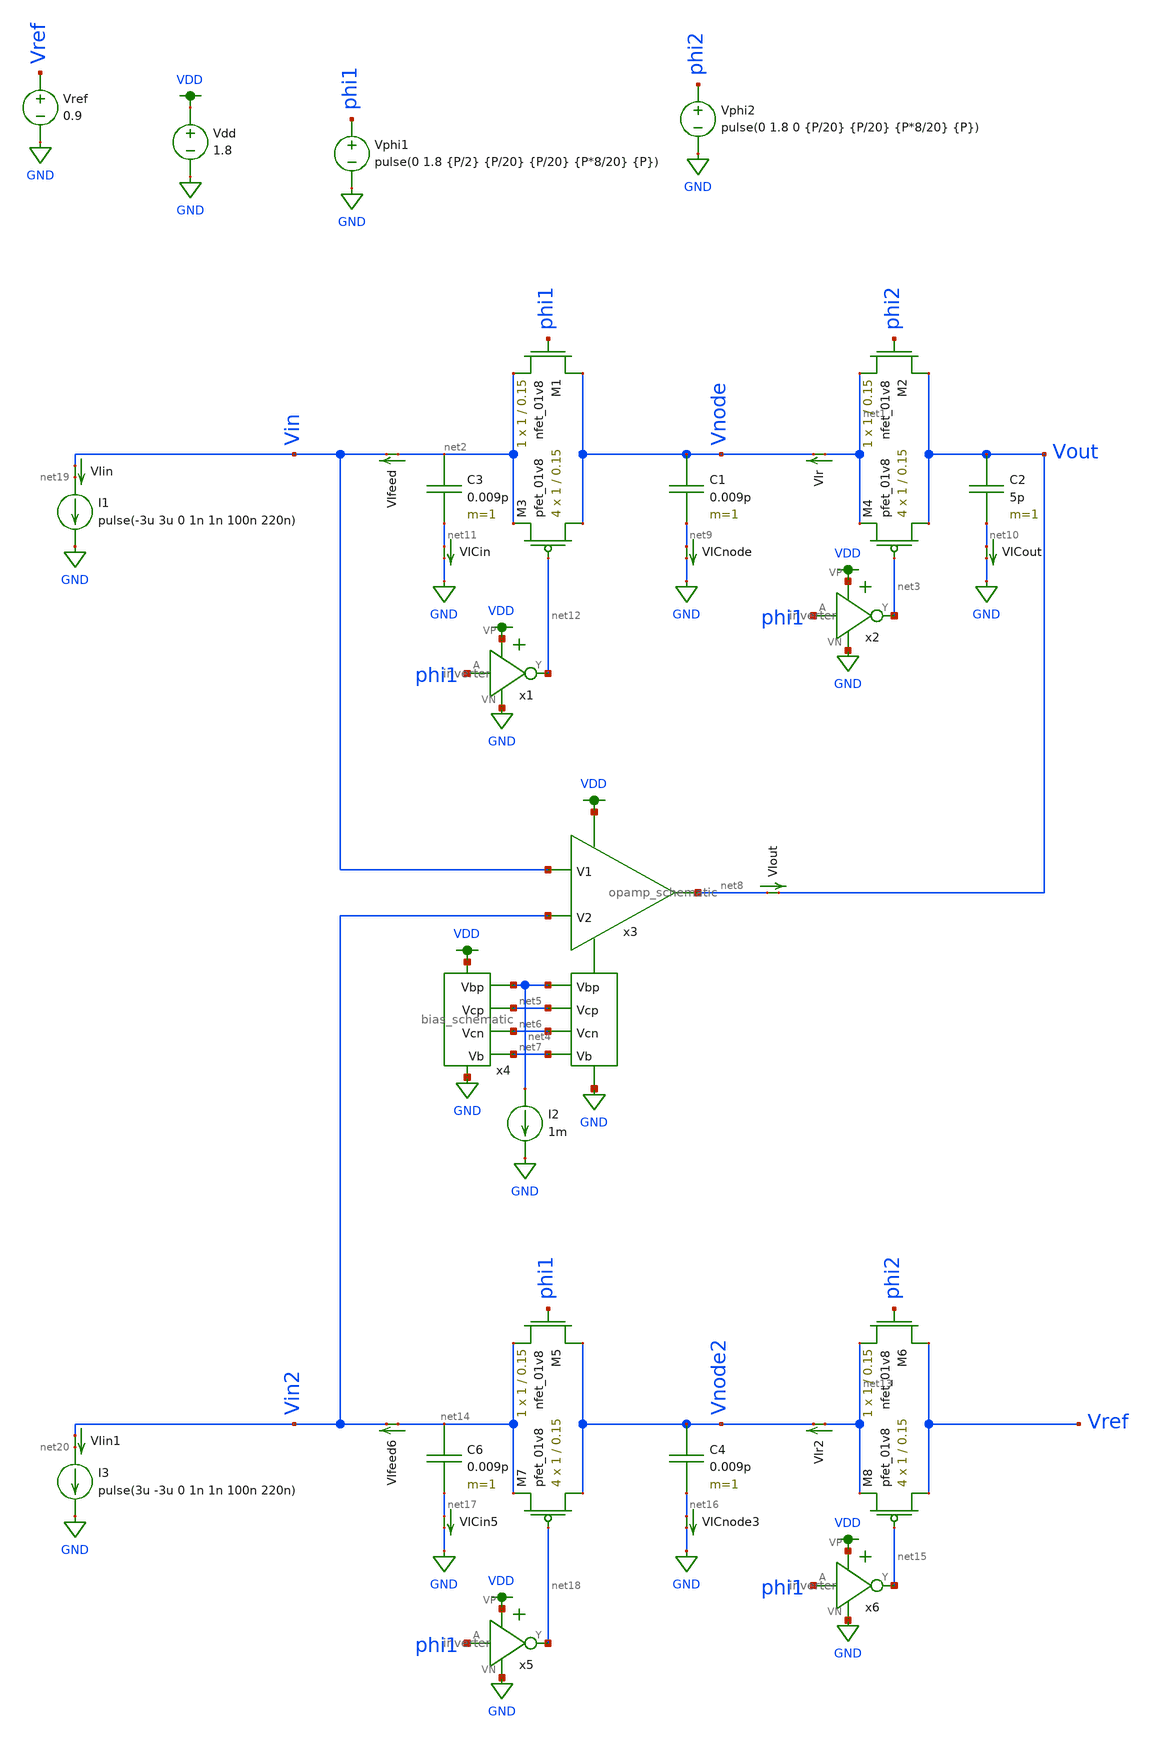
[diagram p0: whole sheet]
** sch_path: xschem/switched_capacitor/switched_capacitor_dual_iv_converter.sch
**.subckt switched_capacitor_dual_iv_converter
C1 Vnode net9 0.009p m=1
XM1 Vnode phi1 net2 GND sky130_fd_pr__nfet_01v8 L=0.15 W=1 nf=1 ad='int((nf+1)/2) * W/nf * 0.29' as='int((nf+2)/2) * W/nf * 0.29'
+ pd='2*int((nf+1)/2) * (W/nf + 0.29)' ps='2*int((nf+2)/2) * (W/nf + 0.29)' nrd='0.29 / W' nrs='0.29 / W'
+ sa=0 sb=0 sd=0 mult=1 m=1
XM2 Vout phi2 net1 GND sky130_fd_pr__nfet_01v8 L=0.15 W=1 nf=1 ad='int((nf+1)/2) * W/nf * 0.29' as='int((nf+2)/2) * W/nf * 0.29'
+ pd='2*int((nf+1)/2) * (W/nf + 0.29)' ps='2*int((nf+2)/2) * (W/nf + 0.29)' nrd='0.29 / W' nrs='0.29 / W'
+ sa=0 sb=0 sd=0 mult=1 m=1
Vphi1 phi1 GND pulse(0 1.8 {P/2} {P/20} {P/20} {P*8/20} {P})
Vphi2 phi2 GND pulse(0 1.8 0 {P/20} {P/20} {P*8/20} {P})
Vdd VDD GND 1.8
C2 Vout net10 5p m=1
XM3 Vnode net12 net2 VDD sky130_fd_pr__pfet_01v8 L=0.15 W=1 nf=1 ad='int((nf+1)/2) * W/nf * 0.29' as='int((nf+2)/2) * W/nf * 0.29'
+ pd='2*int((nf+1)/2) * (W/nf + 0.29)' ps='2*int((nf+2)/2) * (W/nf + 0.29)' nrd='0.29 / W' nrs='0.29 / W'
+ sa=0 sb=0 sd=0 mult=4 m=4
XM4 Vout net3 net1 VDD sky130_fd_pr__pfet_01v8 L=0.15 W=1 nf=1 ad='int((nf+1)/2) * W/nf * 0.29' as='int((nf+2)/2) * W/nf * 0.29'
+ pd='2*int((nf+1)/2) * (W/nf + 0.29)' ps='2*int((nf+2)/2) * (W/nf + 0.29)' nrd='0.29 / W' nrs='0.29 / W'
+ sa=0 sb=0 sd=0 mult=4 m=4
x1 VDD phi1 net12 GND inverter
x2 VDD phi1 net3 GND inverter
I1 net19 GND pulse(-3u 3u 0 1n 1n 100n 220n)
C3 net2 net11 0.009p m=1
x3 VDD net4 net5 net8 Vin Vin2 net6 net7 GND opamp_schematic
x4 VDD net4 net5 net6 GND net7 bias_schematic
Vref Vref GND 0.9
I2 net4 GND 1m
VIin Vin net19 0
.save i(viin)
VIr net1 Vnode 0
.save i(vir)
VIout net8 Vout 0
.save i(viout)
VICnode net9 GND 0
.save i(vicnode)
VICout net10 GND 0
.save i(vicout)
VICin net11 GND 0
.save i(vicin)
VIfeed net2 Vin 0
.save i(vifeed)
C4 Vnode2 net16 0.009p m=1
XM5 Vnode2 phi1 net14 GND sky130_fd_pr__nfet_01v8 L=0.15 W=1 nf=1 ad='int((nf+1)/2) * W/nf * 0.29' as='int((nf+2)/2) * W/nf * 0.29'
+ pd='2*int((nf+1)/2) * (W/nf + 0.29)' ps='2*int((nf+2)/2) * (W/nf + 0.29)' nrd='0.29 / W' nrs='0.29 / W'
+ sa=0 sb=0 sd=0 mult=1 m=1
XM6 Vref phi2 net13 GND sky130_fd_pr__nfet_01v8 L=0.15 W=1 nf=1 ad='int((nf+1)/2) * W/nf * 0.29' as='int((nf+2)/2) * W/nf * 0.29'
+ pd='2*int((nf+1)/2) * (W/nf + 0.29)' ps='2*int((nf+2)/2) * (W/nf + 0.29)' nrd='0.29 / W' nrs='0.29 / W'
+ sa=0 sb=0 sd=0 mult=1 m=1
XM7 Vnode2 net18 net14 VDD sky130_fd_pr__pfet_01v8 L=0.15 W=1 nf=1 ad='int((nf+1)/2) * W/nf * 0.29' as='int((nf+2)/2) * W/nf * 0.29'
+ pd='2*int((nf+1)/2) * (W/nf + 0.29)' ps='2*int((nf+2)/2) * (W/nf + 0.29)' nrd='0.29 / W' nrs='0.29 / W'
+ sa=0 sb=0 sd=0 mult=4 m=4
XM8 Vref net15 net13 VDD sky130_fd_pr__pfet_01v8 L=0.15 W=1 nf=1 ad='int((nf+1)/2) * W/nf * 0.29' as='int((nf+2)/2) * W/nf * 0.29'
+ pd='2*int((nf+1)/2) * (W/nf + 0.29)' ps='2*int((nf+2)/2) * (W/nf + 0.29)' nrd='0.29 / W' nrs='0.29 / W'
+ sa=0 sb=0 sd=0 mult=4 m=4
x5 VDD phi1 net18 GND inverter
x6 VDD phi1 net15 GND inverter
I3 net20 GND pulse(3u -3u 0 1n 1n 100n 220n)
C6 net14 net17 0.009p m=1
VIin1 Vin2 net20 0
.save i(viin1)
VIr2 net13 Vnode2 0
.save i(vir2)
VICnode3 net16 GND 0
.save i(vicnode3)
VICin5 net17 GND 0
.save i(vicin5)
VIfeed6 net14 Vin2 0
.save i(vifeed6)
**** begin user architecture code

.option wnflag=1
.param MC_SWITCH=0.0
.lib ~/skywater/skywater-pdk/libraries/sky130_fd_pr_ngspice/latest/models/sky130.lib.spice tt


.param P=10n
.save all
.control
save all
nodeset v(Vout)=0.9
tran 0.005n 500n
run
plot v(Vin) v(Vout) v(Vnode) v(phi2)
plot i(VIin) i(VIr)
plot v(Vout) i(VIin)*50000+v(Vref)
plot i(VIin) i(VIfeed) i(VIout)
plot i(VICin) i(VICnode) i(VICout)
.endc

**** end user architecture code
**.ends

* expanding   symbol:  /home/madvlsi/dev/git/magic-dds/xschem/other_project_files/inverter.sym # of
*+ pins=4
** sym_path: xschem/other_project_files/inverter.sym
** sch_path: xschem/other_project_files/inverter.sch
.subckt inverter VP A Y VN
*.iopin VP
*.iopin VN
*.ipin A
*.opin Y
XM1 Y A VN VN sky130_fd_pr__nfet_01v8 L=0.15 W=1 nf=1 ad='int((nf+1)/2) * W/nf * 0.29' as='int((nf+2)/2) * W/nf * 0.29'
+ pd='2*int((nf+1)/2) * (W/nf + 0.29)' ps='2*int((nf+2)/2) * (W/nf + 0.29)' nrd='0.29 / W' nrs='0.29 / W'
+ sa=0 sb=0 sd=0 mult=1 m=1
XM2 Y A VP VP sky130_fd_pr__pfet_01v8 L=0.15 W=4 nf=1 ad='int((nf+1)/2) * W/nf * 0.29' as='int((nf+2)/2) * W/nf * 0.29'
+ pd='2*int((nf+1)/2) * (W/nf + 0.29)' ps='2*int((nf+2)/2) * (W/nf + 0.29)' nrd='0.29 / W' nrs='0.29 / W'
+ sa=0 sb=0 sd=0 mult=1 m=1
.ends


* expanding   symbol:
*+  /home/madvlsi/dev/git/magic-dds/xschem/other_project_files/opamp_schematic.sym # of pins=9
** sym_path: xschem/other_project_files/opamp_schematic.sym
** sch_path: xschem/other_project_files/opamp_schematic.sch
.subckt opamp_schematic VP Vbp Vcp Vout V1 V2 Vcn Vb VN
*.ipin Vbp
*.ipin Vcp
*.ipin Vcn
*.ipin V2
*.ipin V1
*.ipin Vb
*.iopin VP
*.iopin VN
*.opin Vout
XM1a M1top V1 Vnode GND sky130_fd_pr__nfet_01v8 L=0.5 W=3 nf=1 ad='int((nf+1)/2) * W/nf * 0.29' as='int((nf+2)/2) * W/nf * 0.29'
+ pd='2*int((nf+1)/2) * (W/nf + 0.29)' ps='2*int((nf+2)/2) * (W/nf + 0.29)' nrd='0.29 / W' nrs='0.29 / W'
+ sa=0 sb=0 sd=0 mult=1 m=1
XM1b M1top V1 Vnode GND sky130_fd_pr__nfet_01v8 L=0.5 W=3 nf=1 ad='int((nf+1)/2) * W/nf * 0.29' as='int((nf+2)/2) * W/nf * 0.29'
+ pd='2*int((nf+1)/2) * (W/nf + 0.29)' ps='2*int((nf+2)/2) * (W/nf + 0.29)' nrd='0.29 / W' nrs='0.29 / W'
+ sa=0 sb=0 sd=0 mult=1 m=1
XM1c M1top V1 Vnode GND sky130_fd_pr__nfet_01v8 L=0.5 W=3 nf=1 ad='int((nf+1)/2) * W/nf * 0.29' as='int((nf+2)/2) * W/nf * 0.29'
+ pd='2*int((nf+1)/2) * (W/nf + 0.29)' ps='2*int((nf+2)/2) * (W/nf + 0.29)' nrd='0.29 / W' nrs='0.29 / W'
+ sa=0 sb=0 sd=0 mult=1 m=1
XM1d M1top V1 Vnode GND sky130_fd_pr__nfet_01v8 L=0.5 W=3 nf=1 ad='int((nf+1)/2) * W/nf * 0.29' as='int((nf+2)/2) * W/nf * 0.29'
+ pd='2*int((nf+1)/2) * (W/nf + 0.29)' ps='2*int((nf+2)/2) * (W/nf + 0.29)' nrd='0.29 / W' nrs='0.29 / W'
+ sa=0 sb=0 sd=0 mult=1 m=1
XM2a M2top V2 Vnode GND sky130_fd_pr__nfet_01v8 L=0.5 W=3 nf=1 ad='int((nf+1)/2) * W/nf * 0.29' as='int((nf+2)/2) * W/nf * 0.29'
+ pd='2*int((nf+1)/2) * (W/nf + 0.29)' ps='2*int((nf+2)/2) * (W/nf + 0.29)' nrd='0.29 / W' nrs='0.29 / W'
+ sa=0 sb=0 sd=0 mult=1 m=1
XM2b M2top V2 Vnode GND sky130_fd_pr__nfet_01v8 L=0.5 W=3 nf=1 ad='int((nf+1)/2) * W/nf * 0.29' as='int((nf+2)/2) * W/nf * 0.29'
+ pd='2*int((nf+1)/2) * (W/nf + 0.29)' ps='2*int((nf+2)/2) * (W/nf + 0.29)' nrd='0.29 / W' nrs='0.29 / W'
+ sa=0 sb=0 sd=0 mult=1 m=1
XM2c M2top V2 Vnode GND sky130_fd_pr__nfet_01v8 L=0.5 W=3 nf=1 ad='int((nf+1)/2) * W/nf * 0.29' as='int((nf+2)/2) * W/nf * 0.29'
+ pd='2*int((nf+1)/2) * (W/nf + 0.29)' ps='2*int((nf+2)/2) * (W/nf + 0.29)' nrd='0.29 / W' nrs='0.29 / W'
+ sa=0 sb=0 sd=0 mult=1 m=1
XM2d M2top V2 Vnode GND sky130_fd_pr__nfet_01v8 L=0.5 W=3 nf=1 ad='int((nf+1)/2) * W/nf * 0.29' as='int((nf+2)/2) * W/nf * 0.29'
+ pd='2*int((nf+1)/2) * (W/nf + 0.29)' ps='2*int((nf+2)/2) * (W/nf + 0.29)' nrd='0.29 / W' nrs='0.29 / W'
+ sa=0 sb=0 sd=0 mult=1 m=1
XMba Vnode Vb VN GND sky130_fd_pr__nfet_01v8 L=0.5 W=1.5 nf=1 ad='int((nf+1)/2) * W/nf * 0.29' as='int((nf+2)/2) * W/nf * 0.29'
+ pd='2*int((nf+1)/2) * (W/nf + 0.29)' ps='2*int((nf+2)/2) * (W/nf + 0.29)' nrd='0.29 / W' nrs='0.29 / W'
+ sa=0 sb=0 sd=0 mult=1 m=1
XMbb Vnode Vb VN GND sky130_fd_pr__nfet_01v8 L=0.5 W=1.5 nf=1 ad='int((nf+1)/2) * W/nf * 0.29' as='int((nf+2)/2) * W/nf * 0.29'
+ pd='2*int((nf+1)/2) * (W/nf + 0.29)' ps='2*int((nf+2)/2) * (W/nf + 0.29)' nrd='0.29 / W' nrs='0.29 / W'
+ sa=0 sb=0 sd=0 mult=1 m=1
XMbc Vnode Vb VN GND sky130_fd_pr__nfet_01v8 L=0.5 W=1.5 nf=1 ad='int((nf+1)/2) * W/nf * 0.29' as='int((nf+2)/2) * W/nf * 0.29'
+ pd='2*int((nf+1)/2) * (W/nf + 0.29)' ps='2*int((nf+2)/2) * (W/nf + 0.29)' nrd='0.29 / W' nrs='0.29 / W'
+ sa=0 sb=0 sd=0 mult=1 m=1
XMbd Vnode Vb VN GND sky130_fd_pr__nfet_01v8 L=0.5 W=1.5 nf=1 ad='int((nf+1)/2) * W/nf * 0.29' as='int((nf+2)/2) * W/nf * 0.29'
+ pd='2*int((nf+1)/2) * (W/nf + 0.29)' ps='2*int((nf+2)/2) * (W/nf + 0.29)' nrd='0.29 / W' nrs='0.29 / W'
+ sa=0 sb=0 sd=0 mult=1 m=1
XMbe Vnode Vb VN GND sky130_fd_pr__nfet_01v8 L=0.5 W=1.5 nf=1 ad='int((nf+1)/2) * W/nf * 0.29' as='int((nf+2)/2) * W/nf * 0.29'
+ pd='2*int((nf+1)/2) * (W/nf + 0.29)' ps='2*int((nf+2)/2) * (W/nf + 0.29)' nrd='0.29 / W' nrs='0.29 / W'
+ sa=0 sb=0 sd=0 mult=1 m=1
XMbf Vnode Vb VN GND sky130_fd_pr__nfet_01v8 L=0.5 W=1.5 nf=1 ad='int((nf+1)/2) * W/nf * 0.29' as='int((nf+2)/2) * W/nf * 0.29'
+ pd='2*int((nf+1)/2) * (W/nf + 0.29)' ps='2*int((nf+2)/2) * (W/nf + 0.29)' nrd='0.29 / W' nrs='0.29 / W'
+ sa=0 sb=0 sd=0 mult=1 m=1
XMbg Vnode Vb VN GND sky130_fd_pr__nfet_01v8 L=0.5 W=1.5 nf=1 ad='int((nf+1)/2) * W/nf * 0.29' as='int((nf+2)/2) * W/nf * 0.29'
+ pd='2*int((nf+1)/2) * (W/nf + 0.29)' ps='2*int((nf+2)/2) * (W/nf + 0.29)' nrd='0.29 / W' nrs='0.29 / W'
+ sa=0 sb=0 sd=0 mult=1 m=1
XMbh Vnode Vb VN GND sky130_fd_pr__nfet_01v8 L=0.5 W=1.5 nf=1 ad='int((nf+1)/2) * W/nf * 0.29' as='int((nf+2)/2) * W/nf * 0.29'
+ pd='2*int((nf+1)/2) * (W/nf + 0.29)' ps='2*int((nf+2)/2) * (W/nf + 0.29)' nrd='0.29 / W' nrs='0.29 / W'
+ sa=0 sb=0 sd=0 mult=1 m=1
XM7a net2 Vcn net1 GND sky130_fd_pr__nfet_01v8 L=0.5 W=3 nf=1 ad='int((nf+1)/2) * W/nf * 0.29' as='int((nf+2)/2) * W/nf * 0.29'
+ pd='2*int((nf+1)/2) * (W/nf + 0.29)' ps='2*int((nf+2)/2) * (W/nf + 0.29)' nrd='0.29 / W' nrs='0.29 / W'
+ sa=0 sb=0 sd=0 mult=1 m=1
XM7b net2 Vcn net1 GND sky130_fd_pr__nfet_01v8 L=0.5 W=3 nf=1 ad='int((nf+1)/2) * W/nf * 0.29' as='int((nf+2)/2) * W/nf * 0.29'
+ pd='2*int((nf+1)/2) * (W/nf + 0.29)' ps='2*int((nf+2)/2) * (W/nf + 0.29)' nrd='0.29 / W' nrs='0.29 / W'
+ sa=0 sb=0 sd=0 mult=1 m=1
XM7c net2 Vcn net1 GND sky130_fd_pr__nfet_01v8 L=0.5 W=3 nf=1 ad='int((nf+1)/2) * W/nf * 0.29' as='int((nf+2)/2) * W/nf * 0.29'
+ pd='2*int((nf+1)/2) * (W/nf + 0.29)' ps='2*int((nf+2)/2) * (W/nf + 0.29)' nrd='0.29 / W' nrs='0.29 / W'
+ sa=0 sb=0 sd=0 mult=1 m=1
XM7d net2 Vcn net1 GND sky130_fd_pr__nfet_01v8 L=0.5 W=3 nf=1 ad='int((nf+1)/2) * W/nf * 0.29' as='int((nf+2)/2) * W/nf * 0.29'
+ pd='2*int((nf+1)/2) * (W/nf + 0.29)' ps='2*int((nf+2)/2) * (W/nf + 0.29)' nrd='0.29 / W' nrs='0.29 / W'
+ sa=0 sb=0 sd=0 mult=1 m=1
XM8a net3 Vcn Vout GND sky130_fd_pr__nfet_01v8 L=0.5 W=3 nf=1 ad='int((nf+1)/2) * W/nf * 0.29' as='int((nf+2)/2) * W/nf * 0.29'
+ pd='2*int((nf+1)/2) * (W/nf + 0.29)' ps='2*int((nf+2)/2) * (W/nf + 0.29)' nrd='0.29 / W' nrs='0.29 / W'
+ sa=0 sb=0 sd=0 mult=1 m=1
XM8b net3 Vcn Vout GND sky130_fd_pr__nfet_01v8 L=0.5 W=3 nf=1 ad='int((nf+1)/2) * W/nf * 0.29' as='int((nf+2)/2) * W/nf * 0.29'
+ pd='2*int((nf+1)/2) * (W/nf + 0.29)' ps='2*int((nf+2)/2) * (W/nf + 0.29)' nrd='0.29 / W' nrs='0.29 / W'
+ sa=0 sb=0 sd=0 mult=1 m=1
XM8c net3 Vcn Vout GND sky130_fd_pr__nfet_01v8 L=0.5 W=3 nf=1 ad='int((nf+1)/2) * W/nf * 0.29' as='int((nf+2)/2) * W/nf * 0.29'
+ pd='2*int((nf+1)/2) * (W/nf + 0.29)' ps='2*int((nf+2)/2) * (W/nf + 0.29)' nrd='0.29 / W' nrs='0.29 / W'
+ sa=0 sb=0 sd=0 mult=1 m=1
XM8d net3 Vcn Vout GND sky130_fd_pr__nfet_01v8 L=0.5 W=3 nf=1 ad='int((nf+1)/2) * W/nf * 0.29' as='int((nf+2)/2) * W/nf * 0.29'
+ pd='2*int((nf+1)/2) * (W/nf + 0.29)' ps='2*int((nf+2)/2) * (W/nf + 0.29)' nrd='0.29 / W' nrs='0.29 / W'
+ sa=0 sb=0 sd=0 mult=1 m=1
XM9a net1 net2 VN GND sky130_fd_pr__nfet_01v8 L=0.5 W=3 nf=1 ad='int((nf+1)/2) * W/nf * 0.29' as='int((nf+2)/2) * W/nf * 0.29'
+ pd='2*int((nf+1)/2) * (W/nf + 0.29)' ps='2*int((nf+2)/2) * (W/nf + 0.29)' nrd='0.29 / W' nrs='0.29 / W'
+ sa=0 sb=0 sd=0 mult=1 m=1
XM9b net1 net2 VN GND sky130_fd_pr__nfet_01v8 L=0.5 W=3 nf=1 ad='int((nf+1)/2) * W/nf * 0.29' as='int((nf+2)/2) * W/nf * 0.29'
+ pd='2*int((nf+1)/2) * (W/nf + 0.29)' ps='2*int((nf+2)/2) * (W/nf + 0.29)' nrd='0.29 / W' nrs='0.29 / W'
+ sa=0 sb=0 sd=0 mult=1 m=1
XM9c net1 net2 VN GND sky130_fd_pr__nfet_01v8 L=0.5 W=3 nf=1 ad='int((nf+1)/2) * W/nf * 0.29' as='int((nf+2)/2) * W/nf * 0.29'
+ pd='2*int((nf+1)/2) * (W/nf + 0.29)' ps='2*int((nf+2)/2) * (W/nf + 0.29)' nrd='0.29 / W' nrs='0.29 / W'
+ sa=0 sb=0 sd=0 mult=1 m=1
XM9d net1 net2 VN GND sky130_fd_pr__nfet_01v8 L=0.5 W=3 nf=1 ad='int((nf+1)/2) * W/nf * 0.29' as='int((nf+2)/2) * W/nf * 0.29'
+ pd='2*int((nf+1)/2) * (W/nf + 0.29)' ps='2*int((nf+2)/2) * (W/nf + 0.29)' nrd='0.29 / W' nrs='0.29 / W'
+ sa=0 sb=0 sd=0 mult=1 m=1
XM10a VN net2 net3 GND sky130_fd_pr__nfet_01v8 L=0.5 W=3 nf=1 ad='int((nf+1)/2) * W/nf * 0.29' as='int((nf+2)/2) * W/nf * 0.29'
+ pd='2*int((nf+1)/2) * (W/nf + 0.29)' ps='2*int((nf+2)/2) * (W/nf + 0.29)' nrd='0.29 / W' nrs='0.29 / W'
+ sa=0 sb=0 sd=0 mult=1 m=1
XM10b VN net2 net3 GND sky130_fd_pr__nfet_01v8 L=0.5 W=3 nf=1 ad='int((nf+1)/2) * W/nf * 0.29' as='int((nf+2)/2) * W/nf * 0.29'
+ pd='2*int((nf+1)/2) * (W/nf + 0.29)' ps='2*int((nf+2)/2) * (W/nf + 0.29)' nrd='0.29 / W' nrs='0.29 / W'
+ sa=0 sb=0 sd=0 mult=1 m=1
XM10c VN net2 net3 GND sky130_fd_pr__nfet_01v8 L=0.5 W=3 nf=1 ad='int((nf+1)/2) * W/nf * 0.29' as='int((nf+2)/2) * W/nf * 0.29'
+ pd='2*int((nf+1)/2) * (W/nf + 0.29)' ps='2*int((nf+2)/2) * (W/nf + 0.29)' nrd='0.29 / W' nrs='0.29 / W'
+ sa=0 sb=0 sd=0 mult=1 m=1
XM1 VN net2 net3 GND sky130_fd_pr__nfet_01v8 L=0.5 W=3 nf=1 ad='int((nf+1)/2) * W/nf * 0.29' as='int((nf+2)/2) * W/nf * 0.29'
+ pd='2*int((nf+1)/2) * (W/nf + 0.29)' ps='2*int((nf+2)/2) * (W/nf + 0.29)' nrd='0.29 / W' nrs='0.29 / W'
+ sa=0 sb=0 sd=0 mult=1 m=1
XM5a net2 Vcp M1top VDD sky130_fd_pr__pfet_01v8 L=0.5 W=3 nf=1 ad='int((nf+1)/2) * W/nf * 0.29' as='int((nf+2)/2) * W/nf * 0.29'
+ pd='2*int((nf+1)/2) * (W/nf + 0.29)' ps='2*int((nf+2)/2) * (W/nf + 0.29)' nrd='0.29 / W' nrs='0.29 / W'
+ sa=0 sb=0 sd=0 mult=1 m=1
XM5b net2 Vcp M1top VDD sky130_fd_pr__pfet_01v8 L=0.5 W=3 nf=1 ad='int((nf+1)/2) * W/nf * 0.29' as='int((nf+2)/2) * W/nf * 0.29'
+ pd='2*int((nf+1)/2) * (W/nf + 0.29)' ps='2*int((nf+2)/2) * (W/nf + 0.29)' nrd='0.29 / W' nrs='0.29 / W'
+ sa=0 sb=0 sd=0 mult=1 m=1
XM5c net2 Vcp M1top VDD sky130_fd_pr__pfet_01v8 L=0.5 W=3 nf=1 ad='int((nf+1)/2) * W/nf * 0.29' as='int((nf+2)/2) * W/nf * 0.29'
+ pd='2*int((nf+1)/2) * (W/nf + 0.29)' ps='2*int((nf+2)/2) * (W/nf + 0.29)' nrd='0.29 / W' nrs='0.29 / W'
+ sa=0 sb=0 sd=0 mult=1 m=1
XM5d net2 Vcp M1top VDD sky130_fd_pr__pfet_01v8 L=0.5 W=3 nf=1 ad='int((nf+1)/2) * W/nf * 0.29' as='int((nf+2)/2) * W/nf * 0.29'
+ pd='2*int((nf+1)/2) * (W/nf + 0.29)' ps='2*int((nf+2)/2) * (W/nf + 0.29)' nrd='0.29 / W' nrs='0.29 / W'
+ sa=0 sb=0 sd=0 mult=1 m=1
XM6a Vout Vcp M2top VDD sky130_fd_pr__pfet_01v8 L=0.5 W=3 nf=1 ad='int((nf+1)/2) * W/nf * 0.29' as='int((nf+2)/2) * W/nf * 0.29'
+ pd='2*int((nf+1)/2) * (W/nf + 0.29)' ps='2*int((nf+2)/2) * (W/nf + 0.29)' nrd='0.29 / W' nrs='0.29 / W'
+ sa=0 sb=0 sd=0 mult=1 m=1
XM6b Vout Vcp M2top VDD sky130_fd_pr__pfet_01v8 L=0.5 W=3 nf=1 ad='int((nf+1)/2) * W/nf * 0.29' as='int((nf+2)/2) * W/nf * 0.29'
+ pd='2*int((nf+1)/2) * (W/nf + 0.29)' ps='2*int((nf+2)/2) * (W/nf + 0.29)' nrd='0.29 / W' nrs='0.29 / W'
+ sa=0 sb=0 sd=0 mult=1 m=1
XM6c Vout Vcp M2top VDD sky130_fd_pr__pfet_01v8 L=0.5 W=3 nf=1 ad='int((nf+1)/2) * W/nf * 0.29' as='int((nf+2)/2) * W/nf * 0.29'
+ pd='2*int((nf+1)/2) * (W/nf + 0.29)' ps='2*int((nf+2)/2) * (W/nf + 0.29)' nrd='0.29 / W' nrs='0.29 / W'
+ sa=0 sb=0 sd=0 mult=1 m=1
XM6d Vout Vcp M2top VDD sky130_fd_pr__pfet_01v8 L=0.5 W=3 nf=1 ad='int((nf+1)/2) * W/nf * 0.29' as='int((nf+2)/2) * W/nf * 0.29'
+ pd='2*int((nf+1)/2) * (W/nf + 0.29)' ps='2*int((nf+2)/2) * (W/nf + 0.29)' nrd='0.29 / W' nrs='0.29 / W'
+ sa=0 sb=0 sd=0 mult=1 m=1
XM3a M1top Vbp VP VDD sky130_fd_pr__pfet_01v8 L=0.5 W=3 nf=1 ad='int((nf+1)/2) * W/nf * 0.29' as='int((nf+2)/2) * W/nf * 0.29'
+ pd='2*int((nf+1)/2) * (W/nf + 0.29)' ps='2*int((nf+2)/2) * (W/nf + 0.29)' nrd='0.29 / W' nrs='0.29 / W'
+ sa=0 sb=0 sd=0 mult=1 m=1
XM3b M1top Vbp VP VDD sky130_fd_pr__pfet_01v8 L=0.5 W=3 nf=1 ad='int((nf+1)/2) * W/nf * 0.29' as='int((nf+2)/2) * W/nf * 0.29'
+ pd='2*int((nf+1)/2) * (W/nf + 0.29)' ps='2*int((nf+2)/2) * (W/nf + 0.29)' nrd='0.29 / W' nrs='0.29 / W'
+ sa=0 sb=0 sd=0 mult=1 m=1
XM3c M1top Vbp VP VDD sky130_fd_pr__pfet_01v8 L=0.5 W=3 nf=1 ad='int((nf+1)/2) * W/nf * 0.29' as='int((nf+2)/2) * W/nf * 0.29'
+ pd='2*int((nf+1)/2) * (W/nf + 0.29)' ps='2*int((nf+2)/2) * (W/nf + 0.29)' nrd='0.29 / W' nrs='0.29 / W'
+ sa=0 sb=0 sd=0 mult=1 m=1
XM3d M1top Vbp VP VDD sky130_fd_pr__pfet_01v8 L=0.5 W=3 nf=1 ad='int((nf+1)/2) * W/nf * 0.29' as='int((nf+2)/2) * W/nf * 0.29'
+ pd='2*int((nf+1)/2) * (W/nf + 0.29)' ps='2*int((nf+2)/2) * (W/nf + 0.29)' nrd='0.29 / W' nrs='0.29 / W'
+ sa=0 sb=0 sd=0 mult=1 m=1
XM4a M2top Vbp VP VDD sky130_fd_pr__pfet_01v8 L=0.5 W=3 nf=1 ad='int((nf+1)/2) * W/nf * 0.29' as='int((nf+2)/2) * W/nf * 0.29'
+ pd='2*int((nf+1)/2) * (W/nf + 0.29)' ps='2*int((nf+2)/2) * (W/nf + 0.29)' nrd='0.29 / W' nrs='0.29 / W'
+ sa=0 sb=0 sd=0 mult=1 m=1
XM4b M2top Vbp VP VDD sky130_fd_pr__pfet_01v8 L=0.5 W=3 nf=1 ad='int((nf+1)/2) * W/nf * 0.29' as='int((nf+2)/2) * W/nf * 0.29'
+ pd='2*int((nf+1)/2) * (W/nf + 0.29)' ps='2*int((nf+2)/2) * (W/nf + 0.29)' nrd='0.29 / W' nrs='0.29 / W'
+ sa=0 sb=0 sd=0 mult=1 m=1
XM4c M2top Vbp VP VDD sky130_fd_pr__pfet_01v8 L=0.5 W=3 nf=1 ad='int((nf+1)/2) * W/nf * 0.29' as='int((nf+2)/2) * W/nf * 0.29'
+ pd='2*int((nf+1)/2) * (W/nf + 0.29)' ps='2*int((nf+2)/2) * (W/nf + 0.29)' nrd='0.29 / W' nrs='0.29 / W'
+ sa=0 sb=0 sd=0 mult=1 m=1
XM4d M2top Vbp VP VDD sky130_fd_pr__pfet_01v8 L=0.5 W=3 nf=1 ad='int((nf+1)/2) * W/nf * 0.29' as='int((nf+2)/2) * W/nf * 0.29'
+ pd='2*int((nf+1)/2) * (W/nf + 0.29)' ps='2*int((nf+2)/2) * (W/nf + 0.29)' nrd='0.29 / W' nrs='0.29 / W'
+ sa=0 sb=0 sd=0 mult=1 m=1
.ends


* expanding   symbol:  /home/madvlsi/dev/git/magic-dds/xschem/other_project_files/bias_schematic.sym
*+ # of pins=6
** sym_path: xschem/other_project_files/bias_schematic.sym
** sch_path: xschem/other_project_files/bias_schematic.sch
.subckt bias_schematic VP Vbp Vcp Vcn VN Vb
*.iopin VP
*.iopin VN
*.opin Vcp
*.iopin Vbp
*.opin Vcn
*.opin Vb
XM1a net2 net2 net1 GND sky130_fd_pr__nfet_01v8 L=0.5 W=3 nf=1 ad='int((nf+1)/2) * W/nf * 0.29' as='int((nf+2)/2) * W/nf * 0.29'
+ pd='2*int((nf+1)/2) * (W/nf + 0.29)' ps='2*int((nf+2)/2) * (W/nf + 0.29)' nrd='0.29 / W' nrs='0.29 / W'
+ sa=0 sb=0 sd=0 mult=1 m=1
XM1b net2 net2 net1 GND sky130_fd_pr__nfet_01v8 L=0.5 W=3 nf=1 ad='int((nf+1)/2) * W/nf * 0.29' as='int((nf+2)/2) * W/nf * 0.29'
+ pd='2*int((nf+1)/2) * (W/nf + 0.29)' ps='2*int((nf+2)/2) * (W/nf + 0.29)' nrd='0.29 / W' nrs='0.29 / W'
+ sa=0 sb=0 sd=0 mult=1 m=1
XM1c net2 net2 net1 GND sky130_fd_pr__nfet_01v8 L=0.5 W=3 nf=1 ad='int((nf+1)/2) * W/nf * 0.29' as='int((nf+2)/2) * W/nf * 0.29'
+ pd='2*int((nf+1)/2) * (W/nf + 0.29)' ps='2*int((nf+2)/2) * (W/nf + 0.29)' nrd='0.29 / W' nrs='0.29 / W'
+ sa=0 sb=0 sd=0 mult=1 m=1
XM1d net2 net2 net1 GND sky130_fd_pr__nfet_01v8 L=0.5 W=3 nf=1 ad='int((nf+1)/2) * W/nf * 0.29' as='int((nf+2)/2) * W/nf * 0.29'
+ pd='2*int((nf+1)/2) * (W/nf + 0.29)' ps='2*int((nf+2)/2) * (W/nf + 0.29)' nrd='0.29 / W' nrs='0.29 / W'
+ sa=0 sb=0 sd=0 mult=1 m=1
XM2a VN net2 net1 GND sky130_fd_pr__nfet_01v8 L=0.5 W=3 nf=1 ad='int((nf+1)/2) * W/nf * 0.29' as='int((nf+2)/2) * W/nf * 0.29'
+ pd='2*int((nf+1)/2) * (W/nf + 0.29)' ps='2*int((nf+2)/2) * (W/nf + 0.29)' nrd='0.29 / W' nrs='0.29 / W'
+ sa=0 sb=0 sd=0 mult=1 m=1
XM2b VN net2 net1 GND sky130_fd_pr__nfet_01v8 L=0.5 W=3 nf=1 ad='int((nf+1)/2) * W/nf * 0.29' as='int((nf+2)/2) * W/nf * 0.29'
+ pd='2*int((nf+1)/2) * (W/nf + 0.29)' ps='2*int((nf+2)/2) * (W/nf + 0.29)' nrd='0.29 / W' nrs='0.29 / W'
+ sa=0 sb=0 sd=0 mult=1 m=1
XM2c VN net2 net1 GND sky130_fd_pr__nfet_01v8 L=0.5 W=3 nf=1 ad='int((nf+1)/2) * W/nf * 0.29' as='int((nf+2)/2) * W/nf * 0.29'
+ pd='2*int((nf+1)/2) * (W/nf + 0.29)' ps='2*int((nf+2)/2) * (W/nf + 0.29)' nrd='0.29 / W' nrs='0.29 / W'
+ sa=0 sb=0 sd=0 mult=1 m=1
XM2d VN net2 net1 GND sky130_fd_pr__nfet_01v8 L=0.5 W=3 nf=1 ad='int((nf+1)/2) * W/nf * 0.29' as='int((nf+2)/2) * W/nf * 0.29'
+ pd='2*int((nf+1)/2) * (W/nf + 0.29)' ps='2*int((nf+2)/2) * (W/nf + 0.29)' nrd='0.29 / W' nrs='0.29 / W'
+ sa=0 sb=0 sd=0 mult=1 m=1
XM3a net2 Vbp net7 VDD sky130_fd_pr__pfet_01v8 L=0.5 W=3 nf=1 ad='int((nf+1)/2) * W/nf * 0.29' as='int((nf+2)/2) * W/nf * 0.29'
+ pd='2*int((nf+1)/2) * (W/nf + 0.29)' ps='2*int((nf+2)/2) * (W/nf + 0.29)' nrd='0.29 / W' nrs='0.29 / W'
+ sa=0 sb=0 sd=0 mult=1 m=1
XM3b net7 Vbp net6 VDD sky130_fd_pr__pfet_01v8 L=0.5 W=3 nf=1 ad='int((nf+1)/2) * W/nf * 0.29' as='int((nf+2)/2) * W/nf * 0.29'
+ pd='2*int((nf+1)/2) * (W/nf + 0.29)' ps='2*int((nf+2)/2) * (W/nf + 0.29)' nrd='0.29 / W' nrs='0.29 / W'
+ sa=0 sb=0 sd=0 mult=1 m=1
XM3c net6 Vbp net5 VDD sky130_fd_pr__pfet_01v8 L=0.5 W=3 nf=1 ad='int((nf+1)/2) * W/nf * 0.29' as='int((nf+2)/2) * W/nf * 0.29'
+ pd='2*int((nf+1)/2) * (W/nf + 0.29)' ps='2*int((nf+2)/2) * (W/nf + 0.29)' nrd='0.29 / W' nrs='0.29 / W'
+ sa=0 sb=0 sd=0 mult=1 m=1
XM3d net5 Vbp VP VDD sky130_fd_pr__pfet_01v8 L=0.5 W=3 nf=1 ad='int((nf+1)/2) * W/nf * 0.29' as='int((nf+2)/2) * W/nf * 0.29'
+ pd='2*int((nf+1)/2) * (W/nf + 0.29)' ps='2*int((nf+2)/2) * (W/nf + 0.29)' nrd='0.29 / W' nrs='0.29 / W'
+ sa=0 sb=0 sd=0 mult=1 m=1
XM4a Vcn Vbp VP VDD sky130_fd_pr__pfet_01v8 L=0.5 W=3 nf=1 ad='int((nf+1)/2) * W/nf * 0.29' as='int((nf+2)/2) * W/nf * 0.29'
+ pd='2*int((nf+1)/2) * (W/nf + 0.29)' ps='2*int((nf+2)/2) * (W/nf + 0.29)' nrd='0.29 / W' nrs='0.29 / W'
+ sa=0 sb=0 sd=0 mult=1 m=1
XM4b Vcn Vbp VP VDD sky130_fd_pr__pfet_01v8 L=0.5 W=3 nf=1 ad='int((nf+1)/2) * W/nf * 0.29' as='int((nf+2)/2) * W/nf * 0.29'
+ pd='2*int((nf+1)/2) * (W/nf + 0.29)' ps='2*int((nf+2)/2) * (W/nf + 0.29)' nrd='0.29 / W' nrs='0.29 / W'
+ sa=0 sb=0 sd=0 mult=1 m=1
XM4c Vcn Vbp VP VDD sky130_fd_pr__pfet_01v8 L=0.5 W=3 nf=1 ad='int((nf+1)/2) * W/nf * 0.29' as='int((nf+2)/2) * W/nf * 0.29'
+ pd='2*int((nf+1)/2) * (W/nf + 0.29)' ps='2*int((nf+2)/2) * (W/nf + 0.29)' nrd='0.29 / W' nrs='0.29 / W'
+ sa=0 sb=0 sd=0 mult=1 m=1
XM4d Vcn Vbp VP VDD sky130_fd_pr__pfet_01v8 L=0.5 W=3 nf=1 ad='int((nf+1)/2) * W/nf * 0.29' as='int((nf+2)/2) * W/nf * 0.29'
+ pd='2*int((nf+1)/2) * (W/nf + 0.29)' ps='2*int((nf+2)/2) * (W/nf + 0.29)' nrd='0.29 / W' nrs='0.29 / W'
+ sa=0 sb=0 sd=0 mult=1 m=1
XM11a VP Vbp Vbp VDD sky130_fd_pr__pfet_01v8 L=0.5 W=3 nf=1 ad='int((nf+1)/2) * W/nf * 0.29' as='int((nf+2)/2) * W/nf * 0.29'
+ pd='2*int((nf+1)/2) * (W/nf + 0.29)' ps='2*int((nf+2)/2) * (W/nf + 0.29)' nrd='0.29 / W' nrs='0.29 / W'
+ sa=0 sb=0 sd=0 mult=1 m=1
XM11b VP Vbp Vbp VDD sky130_fd_pr__pfet_01v8 L=0.5 W=3 nf=1 ad='int((nf+1)/2) * W/nf * 0.29' as='int((nf+2)/2) * W/nf * 0.29'
+ pd='2*int((nf+1)/2) * (W/nf + 0.29)' ps='2*int((nf+2)/2) * (W/nf + 0.29)' nrd='0.29 / W' nrs='0.29 / W'
+ sa=0 sb=0 sd=0 mult=1 m=1
XM11c VP Vbp Vbp VDD sky130_fd_pr__pfet_01v8 L=0.5 W=3 nf=1 ad='int((nf+1)/2) * W/nf * 0.29' as='int((nf+2)/2) * W/nf * 0.29'
+ pd='2*int((nf+1)/2) * (W/nf + 0.29)' ps='2*int((nf+2)/2) * (W/nf + 0.29)' nrd='0.29 / W' nrs='0.29 / W'
+ sa=0 sb=0 sd=0 mult=1 m=1
XM11d VP Vbp Vbp VDD sky130_fd_pr__pfet_01v8 L=0.5 W=3 nf=1 ad='int((nf+1)/2) * W/nf * 0.29' as='int((nf+2)/2) * W/nf * 0.29'
+ pd='2*int((nf+1)/2) * (W/nf + 0.29)' ps='2*int((nf+2)/2) * (W/nf + 0.29)' nrd='0.29 / W' nrs='0.29 / W'
+ sa=0 sb=0 sd=0 mult=1 m=1
XM5a net1 Vcn Vcn GND sky130_fd_pr__nfet_01v8 L=0.5 W=3 nf=1 ad='int((nf+1)/2) * W/nf * 0.29' as='int((nf+2)/2) * W/nf * 0.29'
+ pd='2*int((nf+1)/2) * (W/nf + 0.29)' ps='2*int((nf+2)/2) * (W/nf + 0.29)' nrd='0.29 / W' nrs='0.29 / W'
+ sa=0 sb=0 sd=0 mult=1 m=1
XM5b net1 Vcn Vcn GND sky130_fd_pr__nfet_01v8 L=0.5 W=3 nf=1 ad='int((nf+1)/2) * W/nf * 0.29' as='int((nf+2)/2) * W/nf * 0.29'
+ pd='2*int((nf+1)/2) * (W/nf + 0.29)' ps='2*int((nf+2)/2) * (W/nf + 0.29)' nrd='0.29 / W' nrs='0.29 / W'
+ sa=0 sb=0 sd=0 mult=1 m=1
XM5c net1 Vcn Vcn GND sky130_fd_pr__nfet_01v8 L=0.5 W=3 nf=1 ad='int((nf+1)/2) * W/nf * 0.29' as='int((nf+2)/2) * W/nf * 0.29'
+ pd='2*int((nf+1)/2) * (W/nf + 0.29)' ps='2*int((nf+2)/2) * (W/nf + 0.29)' nrd='0.29 / W' nrs='0.29 / W'
+ sa=0 sb=0 sd=0 mult=1 m=1
XM5d net1 Vcn Vcn GND sky130_fd_pr__nfet_01v8 L=0.5 W=3 nf=1 ad='int((nf+1)/2) * W/nf * 0.29' as='int((nf+2)/2) * W/nf * 0.29'
+ pd='2*int((nf+1)/2) * (W/nf + 0.29)' ps='2*int((nf+2)/2) * (W/nf + 0.29)' nrd='0.29 / W' nrs='0.29 / W'
+ sa=0 sb=0 sd=0 mult=1 m=1
XM8a net10 Vb net3 GND sky130_fd_pr__nfet_01v8 L=0.5 W=3 nf=1 ad='int((nf+1)/2) * W/nf * 0.29' as='int((nf+2)/2) * W/nf * 0.29'
+ pd='2*int((nf+1)/2) * (W/nf + 0.29)' ps='2*int((nf+2)/2) * (W/nf + 0.29)' nrd='0.29 / W' nrs='0.29 / W'
+ sa=0 sb=0 sd=0 mult=1 m=1
XM8b net9 Vb net10 GND sky130_fd_pr__nfet_01v8 L=0.5 W=3 nf=1 ad='int((nf+1)/2) * W/nf * 0.29' as='int((nf+2)/2) * W/nf * 0.29'
+ pd='2*int((nf+1)/2) * (W/nf + 0.29)' ps='2*int((nf+2)/2) * (W/nf + 0.29)' nrd='0.29 / W' nrs='0.29 / W'
+ sa=0 sb=0 sd=0 mult=1 m=1
XM8c net8 Vb net9 GND sky130_fd_pr__nfet_01v8 L=0.5 W=3 nf=1 ad='int((nf+1)/2) * W/nf * 0.29' as='int((nf+2)/2) * W/nf * 0.29'
+ pd='2*int((nf+1)/2) * (W/nf + 0.29)' ps='2*int((nf+2)/2) * (W/nf + 0.29)' nrd='0.29 / W' nrs='0.29 / W'
+ sa=0 sb=0 sd=0 mult=1 m=1
XM8d VN Vb net8 GND sky130_fd_pr__nfet_01v8 L=0.5 W=3 nf=1 ad='int((nf+1)/2) * W/nf * 0.29' as='int((nf+2)/2) * W/nf * 0.29'
+ pd='2*int((nf+1)/2) * (W/nf + 0.29)' ps='2*int((nf+2)/2) * (W/nf + 0.29)' nrd='0.29 / W' nrs='0.29 / W'
+ sa=0 sb=0 sd=0 mult=1 m=1
XM6a net3 net3 net4 VDD sky130_fd_pr__pfet_01v8 L=0.5 W=3 nf=1 ad='int((nf+1)/2) * W/nf * 0.29' as='int((nf+2)/2) * W/nf * 0.29'
+ pd='2*int((nf+1)/2) * (W/nf + 0.29)' ps='2*int((nf+2)/2) * (W/nf + 0.29)' nrd='0.29 / W' nrs='0.29 / W'
+ sa=0 sb=0 sd=0 mult=1 m=1
XM6b net3 net3 net4 VDD sky130_fd_pr__pfet_01v8 L=0.5 W=3 nf=1 ad='int((nf+1)/2) * W/nf * 0.29' as='int((nf+2)/2) * W/nf * 0.29'
+ pd='2*int((nf+1)/2) * (W/nf + 0.29)' ps='2*int((nf+2)/2) * (W/nf + 0.29)' nrd='0.29 / W' nrs='0.29 / W'
+ sa=0 sb=0 sd=0 mult=1 m=1
XM6c net3 net3 net4 VDD sky130_fd_pr__pfet_01v8 L=0.5 W=3 nf=1 ad='int((nf+1)/2) * W/nf * 0.29' as='int((nf+2)/2) * W/nf * 0.29'
+ pd='2*int((nf+1)/2) * (W/nf + 0.29)' ps='2*int((nf+2)/2) * (W/nf + 0.29)' nrd='0.29 / W' nrs='0.29 / W'
+ sa=0 sb=0 sd=0 mult=1 m=1
XM6d net3 net3 net4 VDD sky130_fd_pr__pfet_01v8 L=0.5 W=3 nf=1 ad='int((nf+1)/2) * W/nf * 0.29' as='int((nf+2)/2) * W/nf * 0.29'
+ pd='2*int((nf+1)/2) * (W/nf + 0.29)' ps='2*int((nf+2)/2) * (W/nf + 0.29)' nrd='0.29 / W' nrs='0.29 / W'
+ sa=0 sb=0 sd=0 mult=1 m=1
XM7a net4 net3 VP VDD sky130_fd_pr__pfet_01v8 L=0.5 W=3 nf=1 ad='int((nf+1)/2) * W/nf * 0.29' as='int((nf+2)/2) * W/nf * 0.29'
+ pd='2*int((nf+1)/2) * (W/nf + 0.29)' ps='2*int((nf+2)/2) * (W/nf + 0.29)' nrd='0.29 / W' nrs='0.29 / W'
+ sa=0 sb=0 sd=0 mult=1 m=1
XM7b net4 net3 VP VDD sky130_fd_pr__pfet_01v8 L=0.5 W=3 nf=1 ad='int((nf+1)/2) * W/nf * 0.29' as='int((nf+2)/2) * W/nf * 0.29'
+ pd='2*int((nf+1)/2) * (W/nf + 0.29)' ps='2*int((nf+2)/2) * (W/nf + 0.29)' nrd='0.29 / W' nrs='0.29 / W'
+ sa=0 sb=0 sd=0 mult=1 m=1
XM7c net4 net3 VP VDD sky130_fd_pr__pfet_01v8 L=0.5 W=3 nf=1 ad='int((nf+1)/2) * W/nf * 0.29' as='int((nf+2)/2) * W/nf * 0.29'
+ pd='2*int((nf+1)/2) * (W/nf + 0.29)' ps='2*int((nf+2)/2) * (W/nf + 0.29)' nrd='0.29 / W' nrs='0.29 / W'
+ sa=0 sb=0 sd=0 mult=1 m=1
XM7d net4 net3 VP VDD sky130_fd_pr__pfet_01v8 L=0.5 W=3 nf=1 ad='int((nf+1)/2) * W/nf * 0.29' as='int((nf+2)/2) * W/nf * 0.29'
+ pd='2*int((nf+1)/2) * (W/nf + 0.29)' ps='2*int((nf+2)/2) * (W/nf + 0.29)' nrd='0.29 / W' nrs='0.29 / W'
+ sa=0 sb=0 sd=0 mult=1 m=1
XM10d net4 Vcp Vcp VDD sky130_fd_pr__pfet_01v8 L=0.5 W=3 nf=1 ad='int((nf+1)/2) * W/nf * 0.29' as='int((nf+2)/2) * W/nf * 0.29'
+ pd='2*int((nf+1)/2) * (W/nf + 0.29)' ps='2*int((nf+2)/2) * (W/nf + 0.29)' nrd='0.29 / W' nrs='0.29 / W'
+ sa=0 sb=0 sd=0 mult=1 m=1
XM10c net4 Vcp Vcp VDD sky130_fd_pr__pfet_01v8 L=0.5 W=3 nf=1 ad='int((nf+1)/2) * W/nf * 0.29' as='int((nf+2)/2) * W/nf * 0.29'
+ pd='2*int((nf+1)/2) * (W/nf + 0.29)' ps='2*int((nf+2)/2) * (W/nf + 0.29)' nrd='0.29 / W' nrs='0.29 / W'
+ sa=0 sb=0 sd=0 mult=1 m=1
XM10b net4 Vcp Vcp VDD sky130_fd_pr__pfet_01v8 L=0.5 W=3 nf=1 ad='int((nf+1)/2) * W/nf * 0.29' as='int((nf+2)/2) * W/nf * 0.29'
+ pd='2*int((nf+1)/2) * (W/nf + 0.29)' ps='2*int((nf+2)/2) * (W/nf + 0.29)' nrd='0.29 / W' nrs='0.29 / W'
+ sa=0 sb=0 sd=0 mult=1 m=1
XM10a net4 Vcp Vcp VDD sky130_fd_pr__pfet_01v8 L=0.5 W=3 nf=1 ad='int((nf+1)/2) * W/nf * 0.29' as='int((nf+2)/2) * W/nf * 0.29'
+ pd='2*int((nf+1)/2) * (W/nf + 0.29)' ps='2*int((nf+2)/2) * (W/nf + 0.29)' nrd='0.29 / W' nrs='0.29 / W'
+ sa=0 sb=0 sd=0 mult=1 m=1
XM9a VN Vb Vcp GND sky130_fd_pr__nfet_01v8 L=0.5 W=3 nf=1 ad='int((nf+1)/2) * W/nf * 0.29' as='int((nf+2)/2) * W/nf * 0.29'
+ pd='2*int((nf+1)/2) * (W/nf + 0.29)' ps='2*int((nf+2)/2) * (W/nf + 0.29)' nrd='0.29 / W' nrs='0.29 / W'
+ sa=0 sb=0 sd=0 mult=1 m=1
XM9b VN Vb Vcp GND sky130_fd_pr__nfet_01v8 L=0.5 W=3 nf=1 ad='int((nf+1)/2) * W/nf * 0.29' as='int((nf+2)/2) * W/nf * 0.29'
+ pd='2*int((nf+1)/2) * (W/nf + 0.29)' ps='2*int((nf+2)/2) * (W/nf + 0.29)' nrd='0.29 / W' nrs='0.29 / W'
+ sa=0 sb=0 sd=0 mult=1 m=1
XM9c VN Vb Vcp GND sky130_fd_pr__nfet_01v8 L=0.5 W=3 nf=1 ad='int((nf+1)/2) * W/nf * 0.29' as='int((nf+2)/2) * W/nf * 0.29'
+ pd='2*int((nf+1)/2) * (W/nf + 0.29)' ps='2*int((nf+2)/2) * (W/nf + 0.29)' nrd='0.29 / W' nrs='0.29 / W'
+ sa=0 sb=0 sd=0 mult=1 m=1
XM9d VN Vb Vcp GND sky130_fd_pr__nfet_01v8 L=0.5 W=3 nf=1 ad='int((nf+1)/2) * W/nf * 0.29' as='int((nf+2)/2) * W/nf * 0.29'
+ pd='2*int((nf+1)/2) * (W/nf + 0.29)' ps='2*int((nf+2)/2) * (W/nf + 0.29)' nrd='0.29 / W' nrs='0.29 / W'
+ sa=0 sb=0 sd=0 mult=1 m=1
XM12a VN Vb Vb GND sky130_fd_pr__nfet_01v8 L=0.5 W=3 nf=1 ad='int((nf+1)/2) * W/nf * 0.29' as='int((nf+2)/2) * W/nf * 0.29'
+ pd='2*int((nf+1)/2) * (W/nf + 0.29)' ps='2*int((nf+2)/2) * (W/nf + 0.29)' nrd='0.29 / W' nrs='0.29 / W'
+ sa=0 sb=0 sd=0 mult=1 m=1
XM12b VN Vb Vb GND sky130_fd_pr__nfet_01v8 L=0.5 W=3 nf=1 ad='int((nf+1)/2) * W/nf * 0.29' as='int((nf+2)/2) * W/nf * 0.29'
+ pd='2*int((nf+1)/2) * (W/nf + 0.29)' ps='2*int((nf+2)/2) * (W/nf + 0.29)' nrd='0.29 / W' nrs='0.29 / W'
+ sa=0 sb=0 sd=0 mult=1 m=1
XM12c VN Vb Vb GND sky130_fd_pr__nfet_01v8 L=0.5 W=3 nf=1 ad='int((nf+1)/2) * W/nf * 0.29' as='int((nf+2)/2) * W/nf * 0.29'
+ pd='2*int((nf+1)/2) * (W/nf + 0.29)' ps='2*int((nf+2)/2) * (W/nf + 0.29)' nrd='0.29 / W' nrs='0.29 / W'
+ sa=0 sb=0 sd=0 mult=1 m=1
XM12d VN Vb Vb GND sky130_fd_pr__nfet_01v8 L=0.5 W=3 nf=1 ad='int((nf+1)/2) * W/nf * 0.29' as='int((nf+2)/2) * W/nf * 0.29'
+ pd='2*int((nf+1)/2) * (W/nf + 0.29)' ps='2*int((nf+2)/2) * (W/nf + 0.29)' nrd='0.29 / W' nrs='0.29 / W'
+ sa=0 sb=0 sd=0 mult=1 m=1
XM1 Vb Vbp VP VDD sky130_fd_pr__pfet_01v8 L=0.5 W=3 nf=1 ad='int((nf+1)/2) * W/nf * 0.29' as='int((nf+2)/2) * W/nf * 0.29'
+ pd='2*int((nf+1)/2) * (W/nf + 0.29)' ps='2*int((nf+2)/2) * (W/nf + 0.29)' nrd='0.29 / W' nrs='0.29 / W'
+ sa=0 sb=0 sd=0 mult=1 m=1
XM2 Vb Vbp VP VDD sky130_fd_pr__pfet_01v8 L=0.5 W=3 nf=1 ad='int((nf+1)/2) * W/nf * 0.29' as='int((nf+2)/2) * W/nf * 0.29'
+ pd='2*int((nf+1)/2) * (W/nf + 0.29)' ps='2*int((nf+2)/2) * (W/nf + 0.29)' nrd='0.29 / W' nrs='0.29 / W'
+ sa=0 sb=0 sd=0 mult=1 m=1
XM3 Vb Vbp VP VDD sky130_fd_pr__pfet_01v8 L=0.5 W=3 nf=1 ad='int((nf+1)/2) * W/nf * 0.29' as='int((nf+2)/2) * W/nf * 0.29'
+ pd='2*int((nf+1)/2) * (W/nf + 0.29)' ps='2*int((nf+2)/2) * (W/nf + 0.29)' nrd='0.29 / W' nrs='0.29 / W'
+ sa=0 sb=0 sd=0 mult=1 m=1
XM4 Vb Vbp VP VDD sky130_fd_pr__pfet_01v8 L=0.5 W=3 nf=1 ad='int((nf+1)/2) * W/nf * 0.29' as='int((nf+2)/2) * W/nf * 0.29'
+ pd='2*int((nf+1)/2) * (W/nf + 0.29)' ps='2*int((nf+2)/2) * (W/nf + 0.29)' nrd='0.29 / W' nrs='0.29 / W'
+ sa=0 sb=0 sd=0 mult=1 m=1
XM1e net2 net2 net1 GND sky130_fd_pr__nfet_01v8 L=0.5 W=3 nf=1 ad='int((nf+1)/2) * W/nf * 0.29' as='int((nf+2)/2) * W/nf * 0.29'
+ pd='2*int((nf+1)/2) * (W/nf + 0.29)' ps='2*int((nf+2)/2) * (W/nf + 0.29)' nrd='0.29 / W' nrs='0.29 / W'
+ sa=0 sb=0 sd=0 mult=1 m=1
XM1f net2 net2 net1 GND sky130_fd_pr__nfet_01v8 L=0.5 W=3 nf=1 ad='int((nf+1)/2) * W/nf * 0.29' as='int((nf+2)/2) * W/nf * 0.29'
+ pd='2*int((nf+1)/2) * (W/nf + 0.29)' ps='2*int((nf+2)/2) * (W/nf + 0.29)' nrd='0.29 / W' nrs='0.29 / W'
+ sa=0 sb=0 sd=0 mult=1 m=1
XM1g net2 net2 net1 GND sky130_fd_pr__nfet_01v8 L=0.5 W=3 nf=1 ad='int((nf+1)/2) * W/nf * 0.29' as='int((nf+2)/2) * W/nf * 0.29'
+ pd='2*int((nf+1)/2) * (W/nf + 0.29)' ps='2*int((nf+2)/2) * (W/nf + 0.29)' nrd='0.29 / W' nrs='0.29 / W'
+ sa=0 sb=0 sd=0 mult=1 m=1
XM1h net2 net2 net1 GND sky130_fd_pr__nfet_01v8 L=0.5 W=3 nf=1 ad='int((nf+1)/2) * W/nf * 0.29' as='int((nf+2)/2) * W/nf * 0.29'
+ pd='2*int((nf+1)/2) * (W/nf + 0.29)' ps='2*int((nf+2)/2) * (W/nf + 0.29)' nrd='0.29 / W' nrs='0.29 / W'
+ sa=0 sb=0 sd=0 mult=1 m=1
XM6e net3 net3 net4 VDD sky130_fd_pr__pfet_01v8 L=0.5 W=3 nf=1 ad='int((nf+1)/2) * W/nf * 0.29' as='int((nf+2)/2) * W/nf * 0.29'
+ pd='2*int((nf+1)/2) * (W/nf + 0.29)' ps='2*int((nf+2)/2) * (W/nf + 0.29)' nrd='0.29 / W' nrs='0.29 / W'
+ sa=0 sb=0 sd=0 mult=1 m=1
XM6f net3 net3 net4 VDD sky130_fd_pr__pfet_01v8 L=0.5 W=3 nf=1 ad='int((nf+1)/2) * W/nf * 0.29' as='int((nf+2)/2) * W/nf * 0.29'
+ pd='2*int((nf+1)/2) * (W/nf + 0.29)' ps='2*int((nf+2)/2) * (W/nf + 0.29)' nrd='0.29 / W' nrs='0.29 / W'
+ sa=0 sb=0 sd=0 mult=1 m=1
XM6g net3 net3 net4 VDD sky130_fd_pr__pfet_01v8 L=0.5 W=3 nf=1 ad='int((nf+1)/2) * W/nf * 0.29' as='int((nf+2)/2) * W/nf * 0.29'
+ pd='2*int((nf+1)/2) * (W/nf + 0.29)' ps='2*int((nf+2)/2) * (W/nf + 0.29)' nrd='0.29 / W' nrs='0.29 / W'
+ sa=0 sb=0 sd=0 mult=1 m=1
XM6h net3 net3 net4 VDD sky130_fd_pr__pfet_01v8 L=0.5 W=3 nf=1 ad='int((nf+1)/2) * W/nf * 0.29' as='int((nf+2)/2) * W/nf * 0.29'
+ pd='2*int((nf+1)/2) * (W/nf + 0.29)' ps='2*int((nf+2)/2) * (W/nf + 0.29)' nrd='0.29 / W' nrs='0.29 / W'
+ sa=0 sb=0 sd=0 mult=1 m=1
XM1i net2 net2 net1 GND sky130_fd_pr__nfet_01v8 L=0.5 W=3 nf=1 ad='int((nf+1)/2) * W/nf * 0.29' as='int((nf+2)/2) * W/nf * 0.29'
+ pd='2*int((nf+1)/2) * (W/nf + 0.29)' ps='2*int((nf+2)/2) * (W/nf + 0.29)' nrd='0.29 / W' nrs='0.29 / W'
+ sa=0 sb=0 sd=0 mult=1 m=1
XM1j net2 net2 net1 GND sky130_fd_pr__nfet_01v8 L=0.5 W=3 nf=1 ad='int((nf+1)/2) * W/nf * 0.29' as='int((nf+2)/2) * W/nf * 0.29'
+ pd='2*int((nf+1)/2) * (W/nf + 0.29)' ps='2*int((nf+2)/2) * (W/nf + 0.29)' nrd='0.29 / W' nrs='0.29 / W'
+ sa=0 sb=0 sd=0 mult=1 m=1
XM1k net2 net2 net1 GND sky130_fd_pr__nfet_01v8 L=0.5 W=3 nf=1 ad='int((nf+1)/2) * W/nf * 0.29' as='int((nf+2)/2) * W/nf * 0.29'
+ pd='2*int((nf+1)/2) * (W/nf + 0.29)' ps='2*int((nf+2)/2) * (W/nf + 0.29)' nrd='0.29 / W' nrs='0.29 / W'
+ sa=0 sb=0 sd=0 mult=1 m=1
XM1l net2 net2 net1 GND sky130_fd_pr__nfet_01v8 L=0.5 W=3 nf=1 ad='int((nf+1)/2) * W/nf * 0.29' as='int((nf+2)/2) * W/nf * 0.29'
+ pd='2*int((nf+1)/2) * (W/nf + 0.29)' ps='2*int((nf+2)/2) * (W/nf + 0.29)' nrd='0.29 / W' nrs='0.29 / W'
+ sa=0 sb=0 sd=0 mult=1 m=1
XM6i net3 net3 net4 VDD sky130_fd_pr__pfet_01v8 L=0.5 W=3 nf=1 ad='int((nf+1)/2) * W/nf * 0.29' as='int((nf+2)/2) * W/nf * 0.29'
+ pd='2*int((nf+1)/2) * (W/nf + 0.29)' ps='2*int((nf+2)/2) * (W/nf + 0.29)' nrd='0.29 / W' nrs='0.29 / W'
+ sa=0 sb=0 sd=0 mult=1 m=1
XM6j net3 net3 net4 VDD sky130_fd_pr__pfet_01v8 L=0.5 W=3 nf=1 ad='int((nf+1)/2) * W/nf * 0.29' as='int((nf+2)/2) * W/nf * 0.29'
+ pd='2*int((nf+1)/2) * (W/nf + 0.29)' ps='2*int((nf+2)/2) * (W/nf + 0.29)' nrd='0.29 / W' nrs='0.29 / W'
+ sa=0 sb=0 sd=0 mult=1 m=1
XM6k net3 net3 net4 VDD sky130_fd_pr__pfet_01v8 L=0.5 W=3 nf=1 ad='int((nf+1)/2) * W/nf * 0.29' as='int((nf+2)/2) * W/nf * 0.29'
+ pd='2*int((nf+1)/2) * (W/nf + 0.29)' ps='2*int((nf+2)/2) * (W/nf + 0.29)' nrd='0.29 / W' nrs='0.29 / W'
+ sa=0 sb=0 sd=0 mult=1 m=1
XM6l net3 net3 net4 VDD sky130_fd_pr__pfet_01v8 L=0.5 W=3 nf=1 ad='int((nf+1)/2) * W/nf * 0.29' as='int((nf+2)/2) * W/nf * 0.29'
+ pd='2*int((nf+1)/2) * (W/nf + 0.29)' ps='2*int((nf+2)/2) * (W/nf + 0.29)' nrd='0.29 / W' nrs='0.29 / W'
+ sa=0 sb=0 sd=0 mult=1 m=1
.ends

.GLOBAL VDD
.GLOBAL GND
.end
